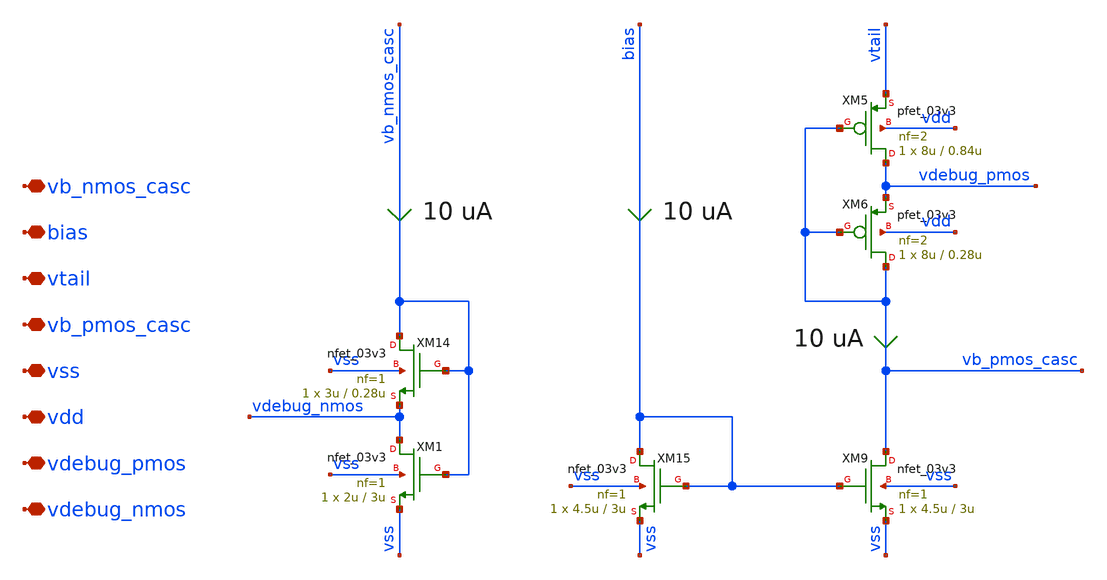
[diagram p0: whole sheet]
** sch_path: xschem/ccia_rrl_ota/b9_ccia_rrl_ota_cascode_bias.sch
**.subckt b9_ccia_rrl_ota_cascode_bias vb_nmos_casc bias vtail vb_pmos_casc vss vdd vdebug_pmos
*+ vdebug_nmos
*.iopin vb_nmos_casc
*.iopin bias
*.iopin vtail
*.iopin vb_pmos_casc
*.iopin vss
*.iopin vdd
*.iopin vdebug_pmos
*.iopin vdebug_nmos
XM1 vdebug_nmos vb_nmos_casc vss vss nfet_03v3 L=3u W=2u nf=1 ad='int((nf+1)/2) * W/nf * 0.18u' as='int((nf+2)/2) * W/nf * 0.18u'
+ pd='2*int((nf+1)/2) * (W/nf + 0.18u)' ps='2*int((nf+2)/2) * (W/nf + 0.18u)' nrd='0.18u / W' nrs='0.18u / W'
+ sa=0 sb=0 sd=0 m=1
XM5 vdebug_pmos vb_pmos_casc vtail vdd pfet_03v3 L=0.84u W=8u nf=2 ad='int((nf+1)/2) * W/nf * 0.18u'
+ as='int((nf+2)/2) * W/nf * 0.18u' pd='2*int((nf+1)/2) * (W/nf + 0.18u)' ps='2*int((nf+2)/2) * (W/nf + 0.18u)'
+ nrd='0.18u / W' nrs='0.18u / W' sa=0 sb=0 sd=0 m=1
XM15 bias bias vss vss nfet_03v3 L=3u W=4.5u nf=1 ad='int((nf+1)/2) * W/nf * 0.18u' as='int((nf+2)/2) * W/nf * 0.18u'
+ pd='2*int((nf+1)/2) * (W/nf + 0.18u)' ps='2*int((nf+2)/2) * (W/nf + 0.18u)' nrd='0.18u / W' nrs='0.18u / W'
+ sa=0 sb=0 sd=0 m=1
XM9 vb_pmos_casc bias vss vss nfet_03v3 L=3u W=4.5u nf=1 ad='int((nf+1)/2) * W/nf * 0.18u' as='int((nf+2)/2) * W/nf * 0.18u'
+ pd='2*int((nf+1)/2) * (W/nf + 0.18u)' ps='2*int((nf+2)/2) * (W/nf + 0.18u)' nrd='0.18u / W' nrs='0.18u / W'
+ sa=0 sb=0 sd=0 m=1
XM6 vb_pmos_casc vb_pmos_casc vdebug_pmos vdd pfet_03v3 L=0.28u W=8u nf=2 ad='int((nf+1)/2) * W/nf * 0.18u'
+ as='int((nf+2)/2) * W/nf * 0.18u' pd='2*int((nf+1)/2) * (W/nf + 0.18u)' ps='2*int((nf+2)/2) * (W/nf + 0.18u)'
+ nrd='0.18u / W' nrs='0.18u / W' sa=0 sb=0 sd=0 m=1
XM14 vb_nmos_casc vb_nmos_casc vdebug_nmos vss nfet_03v3 L=0.28u W=3u nf=1 ad='int((nf+1)/2) * W/nf * 0.18u'
+ as='int((nf+2)/2) * W/nf * 0.18u' pd='2*int((nf+1)/2) * (W/nf + 0.18u)' ps='2*int((nf+2)/2) * (W/nf + 0.18u)'
+ nrd='0.18u / W' nrs='0.18u / W' sa=0 sb=0 sd=0 m=1
**.ends
.end
